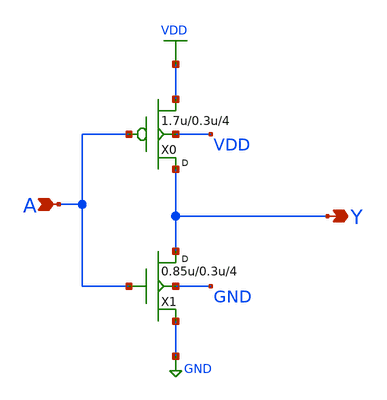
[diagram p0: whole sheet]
** sch_path: gf180mcu_osu_sc_gp12t3v3/cells/clkinv4/gf180mcu_osu_sc_gp12t3v3__clkinv_4.sch
**.subckt gf180mcu_osu_sc_gp12t3v3__clkinv_4 A Y
*.ipin A
*.opin Y
X0 Y A VDD VDD pmos_3p3 w=1.7u l=0.3u m=4
X1 Y A GND GND nmos_3p3 w=0.85u l=0.3u m=4
**.ends
.GLOBAL VDD
.GLOBAL GND
.end
